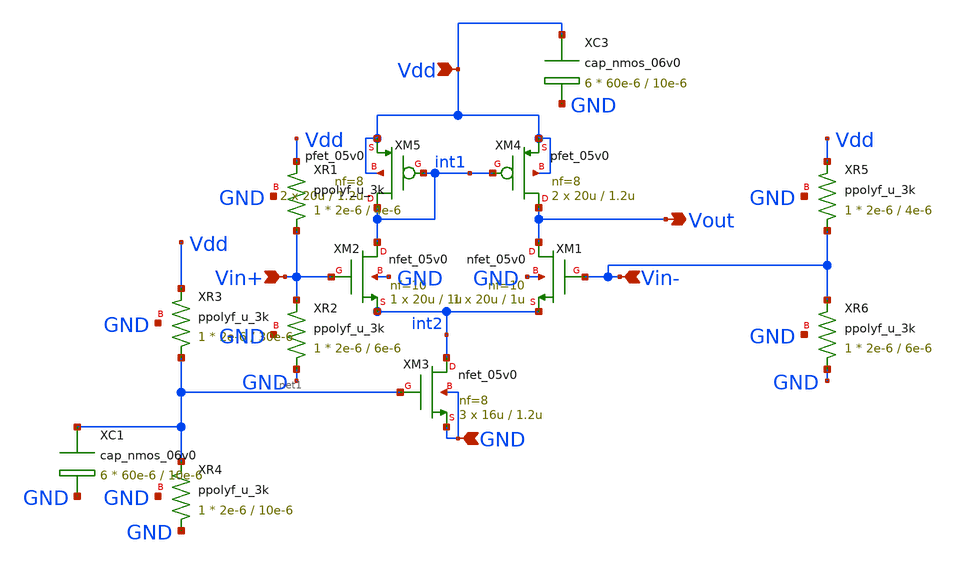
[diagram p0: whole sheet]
** sch_path: RN_Gm2/RN_gm2_ota.sch
**.subckt RN_gm2_ota Vdd GND Vout Vin+ Vin-
*.ipin Vdd
*.ipin GND
*.opin Vout
*.ipin Vin+
*.ipin Vin-
XM1 Vout Vin- int2 GND nfet_05v0 L=1u W=20u nf=10 ad='int((nf+1)/2) * W/nf * 0.18u' as='int((nf+2)/2) * W/nf * 0.18u'
+ pd='2*int((nf+1)/2) * (W/nf + 0.18u)' ps='2*int((nf+2)/2) * (W/nf + 0.18u)' nrd='0.18u / W' nrs='0.18u / W'
+ sa=0 sb=0 sd=0 m=1
XM2 int1 Vin+ int2 GND nfet_05v0 L=1u W=20u nf=10 ad='int((nf+1)/2) * W/nf * 0.18u' as='int((nf+2)/2) * W/nf * 0.18u'
+ pd='2*int((nf+1)/2) * (W/nf + 0.18u)' ps='2*int((nf+2)/2) * (W/nf + 0.18u)' nrd='0.18u / W' nrs='0.18u / W'
+ sa=0 sb=0 sd=0 m=1
XM3 int2 net1 GND GND nfet_05v0 L=1.2u W=16u nf=8 ad='int((nf+1)/2) * W/nf * 0.18u' as='int((nf+2)/2) * W/nf * 0.18u'
+ pd='2*int((nf+1)/2) * (W/nf + 0.18u)' ps='2*int((nf+2)/2) * (W/nf + 0.18u)' nrd='0.18u / W' nrs='0.18u / W'
+ sa=0 sb=0 sd=0 m=3
XM4 Vout int1 Vdd Vdd pfet_05v0 L=1.2u W=20u nf=8 ad='int((nf+1)/2) * W/nf * 0.18u' as='int((nf+2)/2) * W/nf * 0.18u'
+ pd='2*int((nf+1)/2) * (W/nf + 0.18u)' ps='2*int((nf+2)/2) * (W/nf + 0.18u)' nrd='0.18u / W' nrs='0.18u / W'
+ sa=0 sb=0 sd=0 m=2
XM5 int1 int1 Vdd Vdd pfet_05v0 L=1.2u W=20u nf=8 ad='int((nf+1)/2) * W/nf * 0.18u' as='int((nf+2)/2) * W/nf * 0.18u'
+ pd='2*int((nf+1)/2) * (W/nf + 0.18u)' ps='2*int((nf+2)/2) * (W/nf + 0.18u)' nrd='0.18u / W' nrs='0.18u / W'
+ sa=0 sb=0 sd=0 m=2
XR3 net1 Vdd GND ppolyf_u_3k r_width=2e-6 r_length=30e-6 m=1
XR4 GND net1 GND ppolyf_u_3k r_width=2e-6 r_length=10e-6 m=1
XC1 net1 GND cap_nmos_06v0 c_width=60e-6 c_length=10e-6 m=6
XC3 Vdd GND cap_nmos_06v0 c_width=60e-6 c_length=10e-6 m=6
XR5 Vin- Vdd GND ppolyf_u_3k r_width=2e-6 r_length=4e-6 m=1
XR6 GND Vin- GND ppolyf_u_3k r_width=2e-6 r_length=6e-6 m=1
XR1 Vin+ Vdd GND ppolyf_u_3k r_width=2e-6 r_length=4e-6 m=1
XR2 GND Vin+ GND ppolyf_u_3k r_width=2e-6 r_length=6e-6 m=1
**.ends
.end
